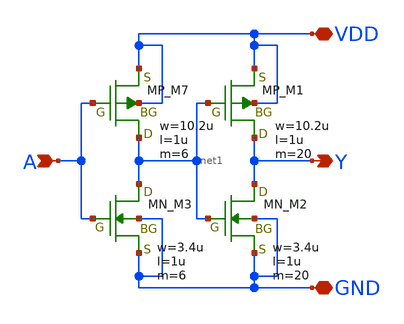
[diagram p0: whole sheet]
** sch_path: libs.tech/xschem/TR-1um_stdcell/CLKBUF_X4.sch
**.subckt CLKBUF_X4 A Y VDD GND
*.ipin A
*.opin Y
*.iopin VDD
*.iopin GND
XM7 net1 A VDD VDD PMOS w=10.2u l=1u nrd=0 nrs=0 m=6
XM1 Y net1 VDD VDD PMOS w=10.2u l=1u nrd=0 nrs=0 m=20
XM3 net1 A GND GND NMOS w=3.4u l=1u nrd=0 nrs=0 m=6
XM2 Y net1 GND GND NMOS w=3.4u l=1u nrd=0 nrs=0 m=20
**.ends
.end
